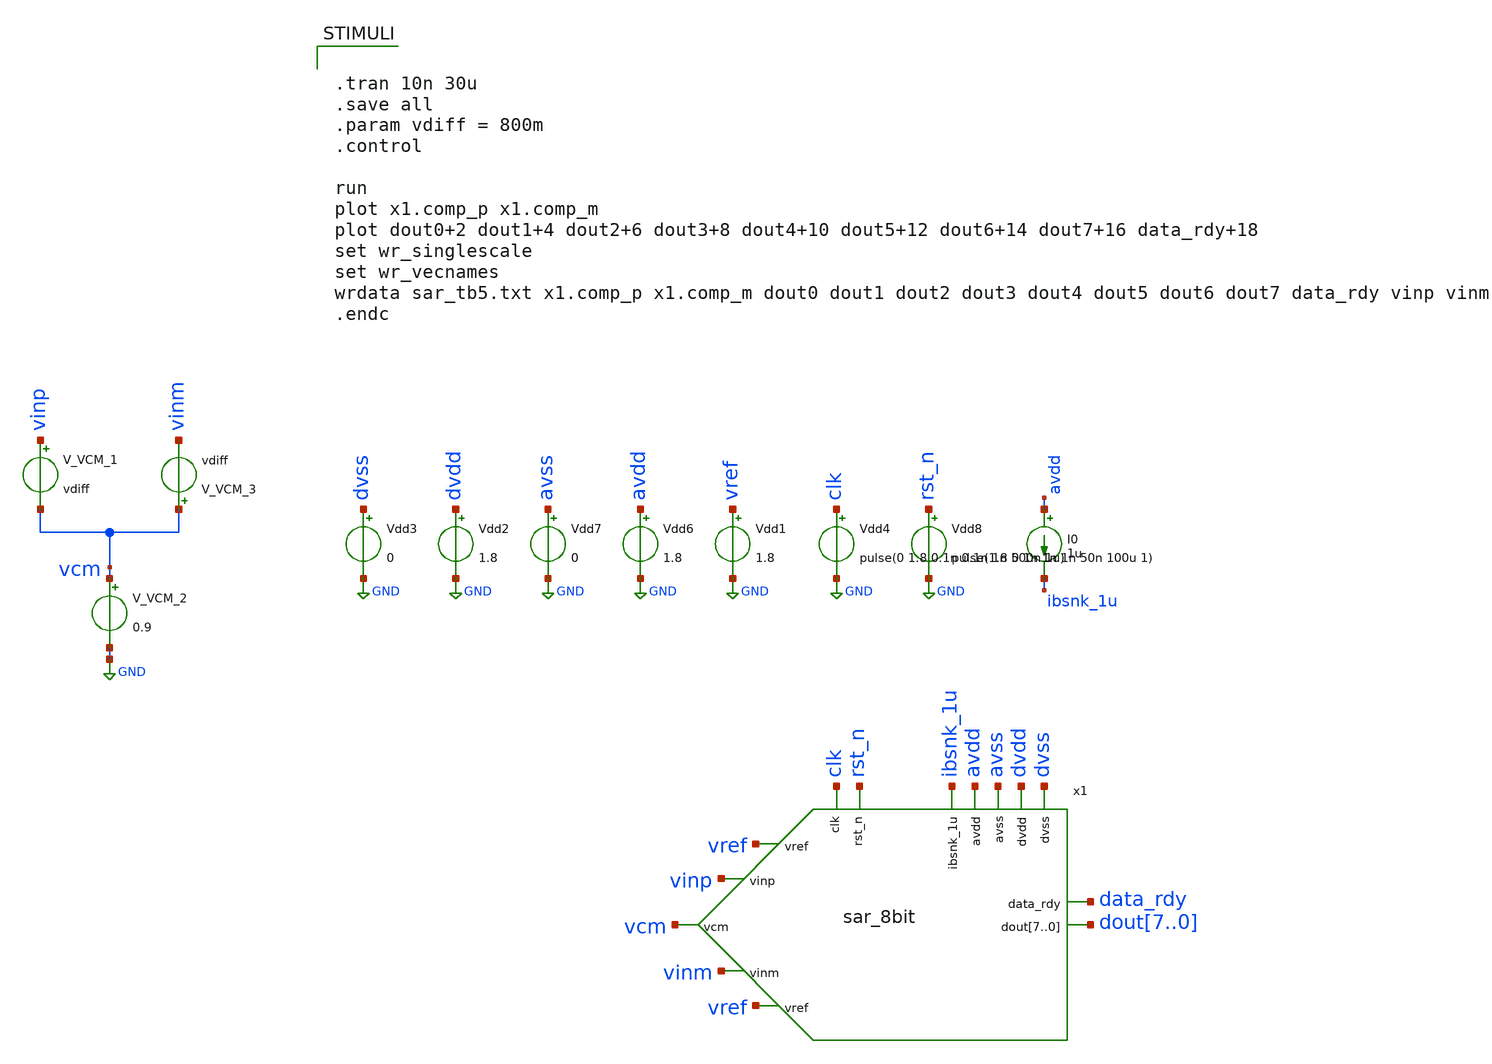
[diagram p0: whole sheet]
** sch_path: test/testbench/sar_tb5.sch
.lib $::SKYWATER_MODELS/sky130.lib.spice tt
.include $::SKYWATER_STDCELLS/sky130_fd_sc_hd.spice

**.subckt sar_tb5
Vdd8 rst_n GND pulse(1.8 0 1n 1n 1n 50n 100u 1)
Vdd4 clk GND pulse(0 1.8 0.1n 0.1n 1n 500n 1u)
Vdd1 vref GND 1.8
V_VCM_2 vcm GND 0.9
V_VCM_1 vinp vcm vdiff
V_VCM_3 vcm vinm vdiff
I0 avdd ibsnk_1u 1u
Vdd2 dvdd GND 1.8
Vdd3 dvss GND 0
Vdd6 avdd GND 1.8
Vdd7 avss GND 0
x1 dout7 dout6 dout5 dout4 dout3 dout2 dout1 dout0 avdd avss data_rdy dvdd dvss vinp vinm vcm vref
+ ibsnk_1u clk rst_n sar_8bit
**** begin user architecture code


.tran 10n 30u
.save all
.param vdiff = 800m
.control

run
plot x1.comp_p x1.comp_m
plot dout0+2 dout1+4 dout2+6 dout3+8 dout4+10 dout5+12 dout6+14 dout7+16 data_rdy+18
set wr_singlescale
set wr_vecnames
wrdata sar_tb5.txt x1.comp_p x1.comp_m dout0 dout1 dout2 dout3 dout4 dout5 dout6 dout7 data_rdy vinp
+ vinm
.endc



.model SWITCH1 sw vt=0.9 vh=0 ron=1 roff =100G

**** end user architecture code
**.ends
.GLOBAL GND
.end
